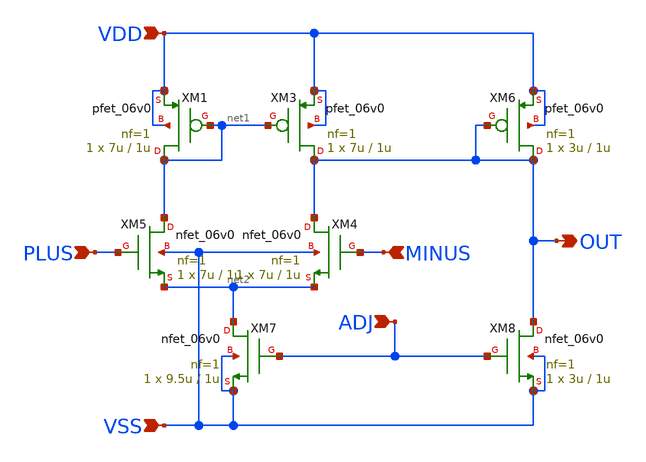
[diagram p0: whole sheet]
** sch_path: macros/Analog/gf180_ntsc/opamp.sch
**.subckt opamp VDD PLUS VSS OUT MINUS ADJ
*.ipin VDD
*.ipin PLUS
*.ipin VSS
*.opin OUT
*.ipin MINUS
*.ipin ADJ
XM1 net1 net1 VDD VDD pfet_06v0 L=1u W=7u nf=1 ad='int((nf+1)/2) * W/nf * 0.18u' as='int((nf+2)/2) * W/nf * 0.18u'
+ pd='2*int((nf+1)/2) * (W/nf + 0.18u)' ps='2*int((nf+2)/2) * (W/nf + 0.18u)' nrd='0.18u / W' nrs='0.18u / W'
+ sa=0 sb=0 sd=0 m=1
XM3 OUT net1 VDD VDD pfet_06v0 L=1u W=7u nf=1 ad='int((nf+1)/2) * W/nf * 0.18u' as='int((nf+2)/2) * W/nf * 0.18u'
+ pd='2*int((nf+1)/2) * (W/nf + 0.18u)' ps='2*int((nf+2)/2) * (W/nf + 0.18u)' nrd='0.18u / W' nrs='0.18u / W'
+ sa=0 sb=0 sd=0 m=1
XM4 OUT MINUS net2 VSS nfet_06v0 L=1u W=7u nf=1 ad='int((nf+1)/2) * W/nf * 0.18u' as='int((nf+2)/2) * W/nf * 0.18u'
+ pd='2*int((nf+1)/2) * (W/nf + 0.18u)' ps='2*int((nf+2)/2) * (W/nf + 0.18u)' nrd='0.18u / W' nrs='0.18u / W'
+ sa=0 sb=0 sd=0 m=1
XM5 net1 PLUS net2 VSS nfet_06v0 L=1u W=7u nf=1 ad='int((nf+1)/2) * W/nf * 0.18u' as='int((nf+2)/2) * W/nf * 0.18u'
+ pd='2*int((nf+1)/2) * (W/nf + 0.18u)' ps='2*int((nf+2)/2) * (W/nf + 0.18u)' nrd='0.18u / W' nrs='0.18u / W'
+ sa=0 sb=0 sd=0 m=1
XM6 OUT OUT VDD VDD pfet_06v0 L=1u W=3u nf=1 ad='int((nf+1)/2) * W/nf * 0.18u' as='int((nf+2)/2) * W/nf * 0.18u'
+ pd='2*int((nf+1)/2) * (W/nf + 0.18u)' ps='2*int((nf+2)/2) * (W/nf + 0.18u)' nrd='0.18u / W' nrs='0.18u / W'
+ sa=0 sb=0 sd=0 m=1
XM7 net2 ADJ VSS VSS nfet_06v0 L=1u W=9.5u nf=1 ad='int((nf+1)/2) * W/nf * 0.18u' as='int((nf+2)/2) * W/nf * 0.18u'
+ pd='2*int((nf+1)/2) * (W/nf + 0.18u)' ps='2*int((nf+2)/2) * (W/nf + 0.18u)' nrd='0.18u / W' nrs='0.18u / W'
+ sa=0 sb=0 sd=0 m=1
XM8 OUT ADJ VSS VSS nfet_06v0 L=1u W=3u nf=1 ad='int((nf+1)/2) * W/nf * 0.18u' as='int((nf+2)/2) * W/nf * 0.18u'
+ pd='2*int((nf+1)/2) * (W/nf + 0.18u)' ps='2*int((nf+2)/2) * (W/nf + 0.18u)' nrd='0.18u / W' nrs='0.18u / W'
+ sa=0 sb=0 sd=0 m=1
**.ends
.end
